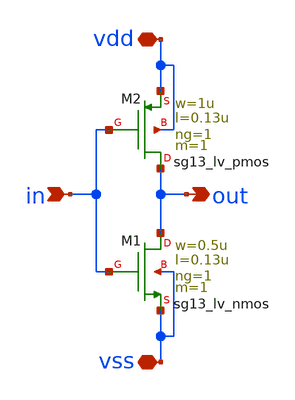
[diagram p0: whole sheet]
** sch_path: SSDOR_1.2V_v2/components/cgenerator/inv.sch
**.subckt inv vdd vss in out
*.iopin vdd
*.iopin vss
*.ipin in
*.opin out
XM1 out in vss vss sg13_lv_nmos w=0.5u l=0.13u ng=1 m=1 mm_ok=1
XM2 out in vdd vdd sg13_lv_pmos w=1u l=0.13u ng=1 m=1 mm_ok=1
**.ends
.end
